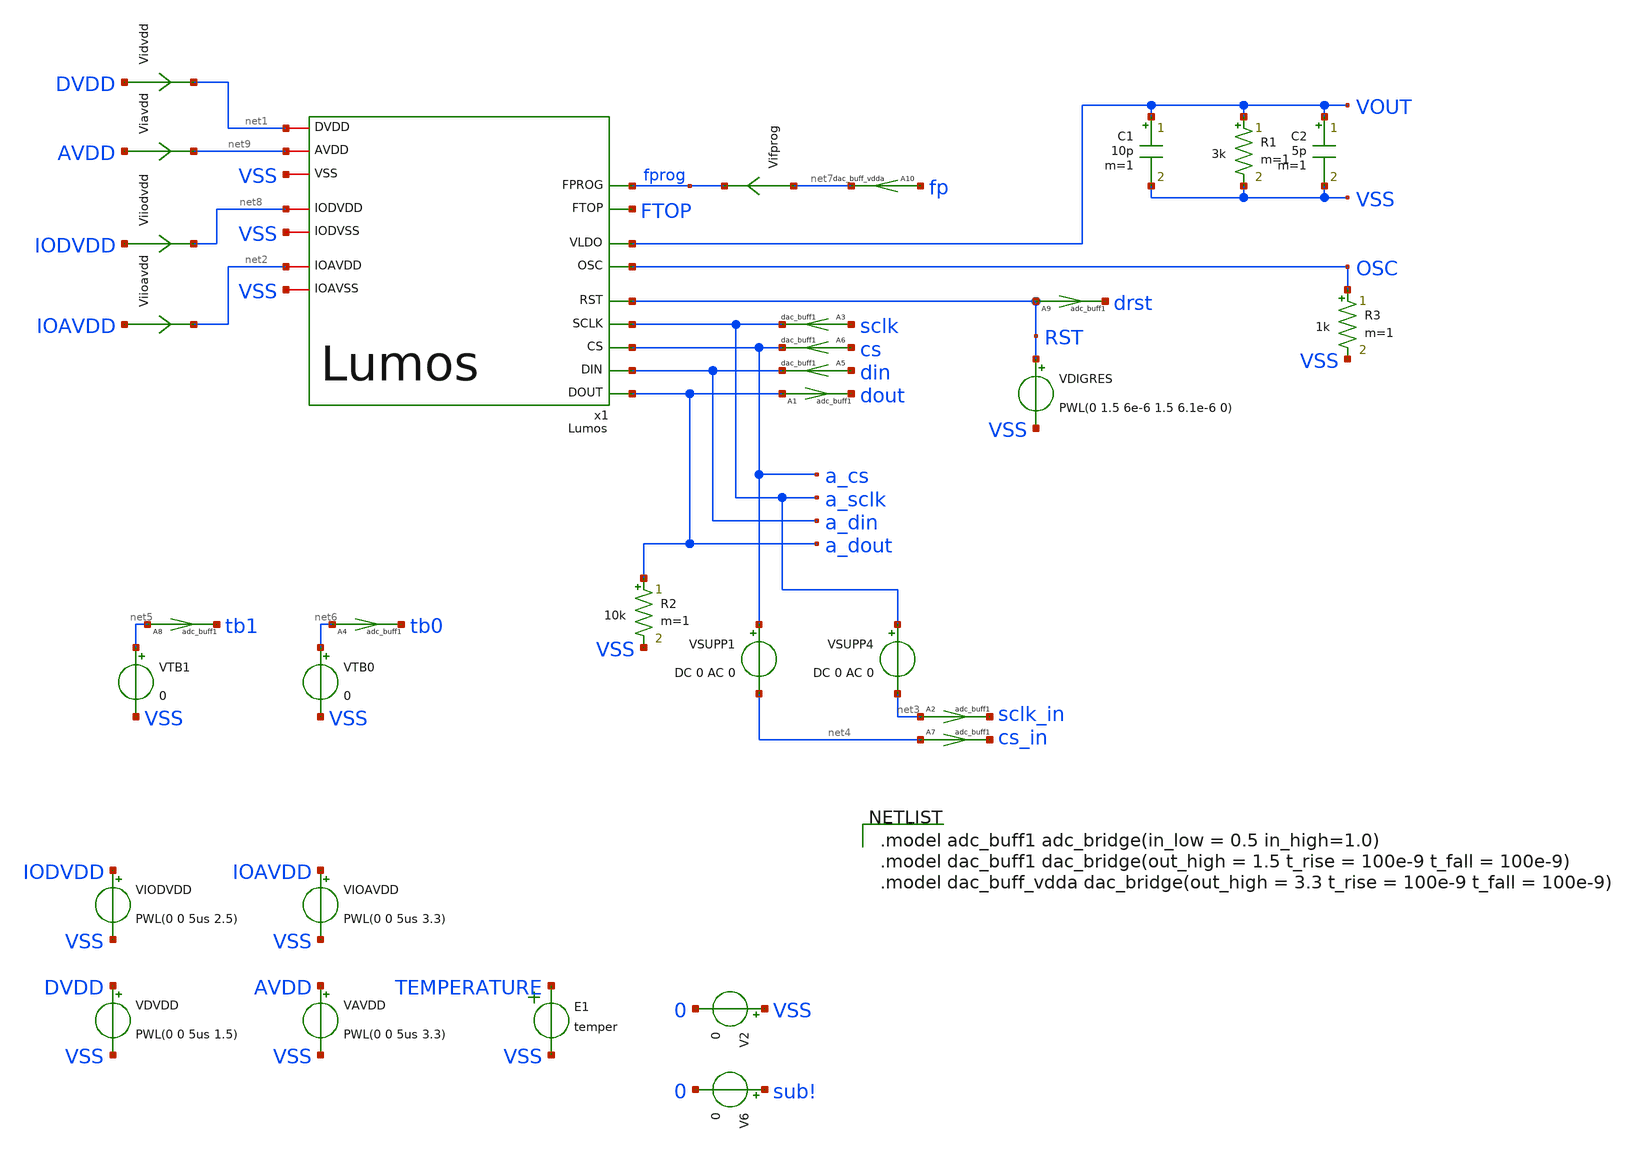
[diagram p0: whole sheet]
** sch_path: xschem/Lumos_tb.sch
**.subckt Lumos_tb
VAVDD AVDD VSS PWL(0 0 5us 3.3)
Viiodvdd IODVDD net8 0
.save i(viiodvdd)
Viavdd AVDD net9 0
.save i(viavdd)
V2 VSS 0 0
E1 TEMPERATURE VSS VOL=' temper '
VDVDD DVDD VSS PWL(0 0 5us 1.5)
C1 VOUT VSS 10p m=1
C2 VOUT VSS 5p m=1
Vidvdd DVDD net1 0
.save i(vidvdd)
V6 sub! 0 0
R3 OSC VSS 1k m=1
VDIGRES RST VSS PWL(0 1.5 6e-6 1.5 6.1e-6 0)
R1 VOUT VSS 3k m=1
VIODVDD IODVDD VSS PWL(0 0 5us 2.5)
VIOAVDD IOAVDD VSS PWL(0 0 5us 3.3)
Viioavdd IOAVDD net2 0
.save i(viioavdd)
A1 [ a_dout ] [ dout ] adc_buff1
A3 [ sclk ] [ a_sclk ] dac_buff1
VSUPP1 a_cs net4 DC 0 AC 0
VSUPP4 a_sclk net3 DC 0 AC 0
A2 [ net3 ] [ sclk_in ] adc_buff1
A7 [ net4 ] [ cs_in ] adc_buff1
A6 [ cs ] [ a_cs ] dac_buff1
A5 [ din ] [ a_din ] dac_buff1
R2 a_dout VSS 10k m=1
VTB0 net6 VSS 0
VTB1 net5 VSS 0
A4 [ net6 ] [ tb0 ] adc_buff1
A8 [ net5 ] [ tb1 ] adc_buff1
A9 [ RST ] [ drst ] adc_buff1
A10 [ fp ] [ net7 ] dac_buff_vdda
Vifprog net7 fprog 0
.save i(vifprog)
x1 net8 net1 VSS VOUT VSS OSC a_sclk RST net9 net2 VSS a_cs a_din a_dout FTOP fprog Lumos
**** begin user architecture code

.csparam TB_ID=${::TB_ID}
.csparam MC_RUNS=${::MC_RUNS}
.csparam EXIT_NGSPICE=${::EXIT_NGSPICE}
.lib ${::IHP_MODELS}/sg13g2.lib ${::CORNER}
.include ${::IHP_MODELS}/sg13g2_esd.lib


* this experimental option enables mos model bin
* selection based on W/NF instead of W
.option wnflag=0

.control
****************************************
* cosimulation model
pre_codemodel /home/lukas/git/asictools/ngspice_cm/codemodels/d_mycosim/d_mycosim.cm
****************************************
* option savecurrents
* save all


* dummy block for goto
if (1)
if TB_ID = 0
	goto TRAN_OSC
end
if TB_ID = 1
	goto TRAN_STARTUP
end
if TB_ID = 2
	goto TRAN_OSC
end
if TB_ID = 3
	goto TRAN_FUSE
end

define max(x,y) (x > y) * x + (x <= y) * y

****************************************
label TRAN_STARTUP
****************************************
if MC_RUNS = 0
	let veclen=27
	let max_i_a = vector(veclen)
	let max_i_d = vector(veclen)
	let max_i_io_a = vector(veclen)
	let max_i_io_d = vector(veclen)
	let ldo_out_over = vector(veclen)
	let ldo_out_end = vector(veclen)
	let temp = vector(veclen)
	let t_supup_a = vector(veclen)
	let t_supup_d = vector(veclen)
	let run = 0

	*foreach te -40 20 140
	foreach te 20
		*foreach t_supup_a 50us 100us 150us
		foreach t_supup_a 100us
			*foreach t_supup_d 50us 100us 150us
			foreach t_supup_d 100us

				.include resources/Lumos_tran_startup_ops.inc

				reset
				let run = run + 1
			end
		end
	end
	set nobreak
	set width=300
	print temp, t_supup_a, t_supup_d, max_i_a, max_i_d, max_i_io_a, max_i_io_d, ldo_out_over,
+ ldo_out_end > tran.csv
else
	let max_i_a = vector(MC_RUNS)
	let max_i_d = vector(MC_RUNS)
	let max_i_io_a = vector(MC_RUNS)
	let max_i_io_d = vector(MC_RUNS)
	let ldo_out_over = vector(MC_RUNS)
	let ldo_out_end = vector(MC_RUNS)
	let temp = vector(MC_RUNS)
	let t_supup_a = vector(MC_RUNS)
	let t_supup_d = vector(MC_RUNS)
	let run=0

	set t_supup_a = 50us
	set t_supup_d = 50us
	set te = 20

	dowhile run < MC_RUNS
		echo MC-RUN: $&run

		.include Lumos_tran_startup_ops.inc

 		reset
		let run = run + 1
	end
	set nobreak
	set width=300
	print temp, t_supup_a, t_supup_d, max_i_a, max_i_d, max_i_io_a, max_i_io_d, ldo_out_over,
+ ldo_out_end > tran.csv
end
goto done

****************************************
label TRAN_OSC
****************************************
if MC_RUNS = 0
	let veclen=3
	let temp = vector(veclen)
	let first_high = vector(veclen)
	let first_period = vector(veclen)
	let first_dutycycle_percent = vector(veclen)
	let last_high = vector(veclen)
	let run = 0

	set t_supup_a = 5us
	set t_supup_d = 5us

	*foreach te -40 20 140
	foreach te 20

		.include resources/Lumos_tran_osc_ops.inc

		reset
		let run = run + 1

	end
	set nobreak
	set width=300
	print temp, first_high, first_period, first_dutycycle_percent > tran.csv
else
	let temp = vector(MC_RUNS)
	let first_high = vector(MC_RUNS)
	let first_period = vector(MC_RUNS)
	let first_dutycycle_percent = vector(MC_RUNS)
	let last_high = vector(MC_RUNS)
	let run=0

	set t_supup_a = 5us
	set t_supup_d = 5us
	set te = 20

	dowhile run < MC_RUNS
		echo MC-RUN: $&run

		.include Lumos_tran_osc_ops.inc

 		reset
		let run = run + 1
	end
	set nobreak
	set width=300
	print temp, first_high, first_period, first_dutycycle_percent > tran.csv
end
goto done

****************************************
label TRAN_FUSE
****************************************
if MC_RUNS = 0
	let veclen=3
	let temp = vector(veclen)
	let max_i = vector(veclen)
	let max_vtop = vector(veclen)
	let run = 0

	set t_supup_a = 5us
	set t_supup_d = 5us

	*foreach te -40 20 140
	foreach te 20

		.include resources/Lumos_tran_fuse_ops.inc

		reset
		let run = run + 1

	end
	set nobreak
	set width=300
	print temp, max_i, max_vtop > tran.csv
else
	let temp = vector(MC_RUNS)
	let max_i = vector(MC_RUNS)
	let max_vtop = vector(MC_RUNS)
	let run=0

	set t_supup_a = 5us
	set t_supup_d = 5us
	set te = 20

	dowhile run < MC_RUNS
		echo MC-RUN: $&run

		.include resources/Lumos_tran_fuse_ops.inc

 		reset
		let run = run + 1
	end
	set nobreak
	set width=300
	print temp, max_i, max_vtop > tran.csv
end
goto done

****************************************
label done
****************************************
if EXIT_NGSPICE > 0.0
	exit
end
end
.endc



.include ${::IHP_PADS}


.model adc_buff1 adc_bridge(in_low = 0.5 in_high=1.0)
.model dac_buff1 dac_bridge(out_high = 1.5 t_rise = 100e-9 t_fall = 100e-9)
.model dac_buff_vdda dac_bridge(out_high = 3.3 t_rise = 100e-9 t_fall = 100e-9)

.model cosim_m d_mycosim (process_file="/usr/bin/python"
+ process_params=["./resources/spi_stimuli.py", "Baud=9600"])
Acontrol [cs_in sclk_in dout drst tb1 tb0] [cs sclk din fp] cosim_m

.include ${::IHP_STDCELLS}/sg13g2_stdcell.spice

.subckt sg13g2_not_1 Y A VDD VSS
XX1 Y A VSS VSS sg13_lv_nmos w=740.00n l=130.00n ng=1 ad=2.516e-13 as=2.516e-13 pd=2.16e-06
+ ps=2.16e-06 m=1
XX0 Y A VDD VDD sg13_lv_pmos w=1.12u l=130.00n ng=1 ad=3.808e-13 as=3.808e-13 pd=2.92e-06
+ ps=2.92e-06 m=1
.ends

**** end user architecture code
**.ends
.GLOBAL sub!
.end
